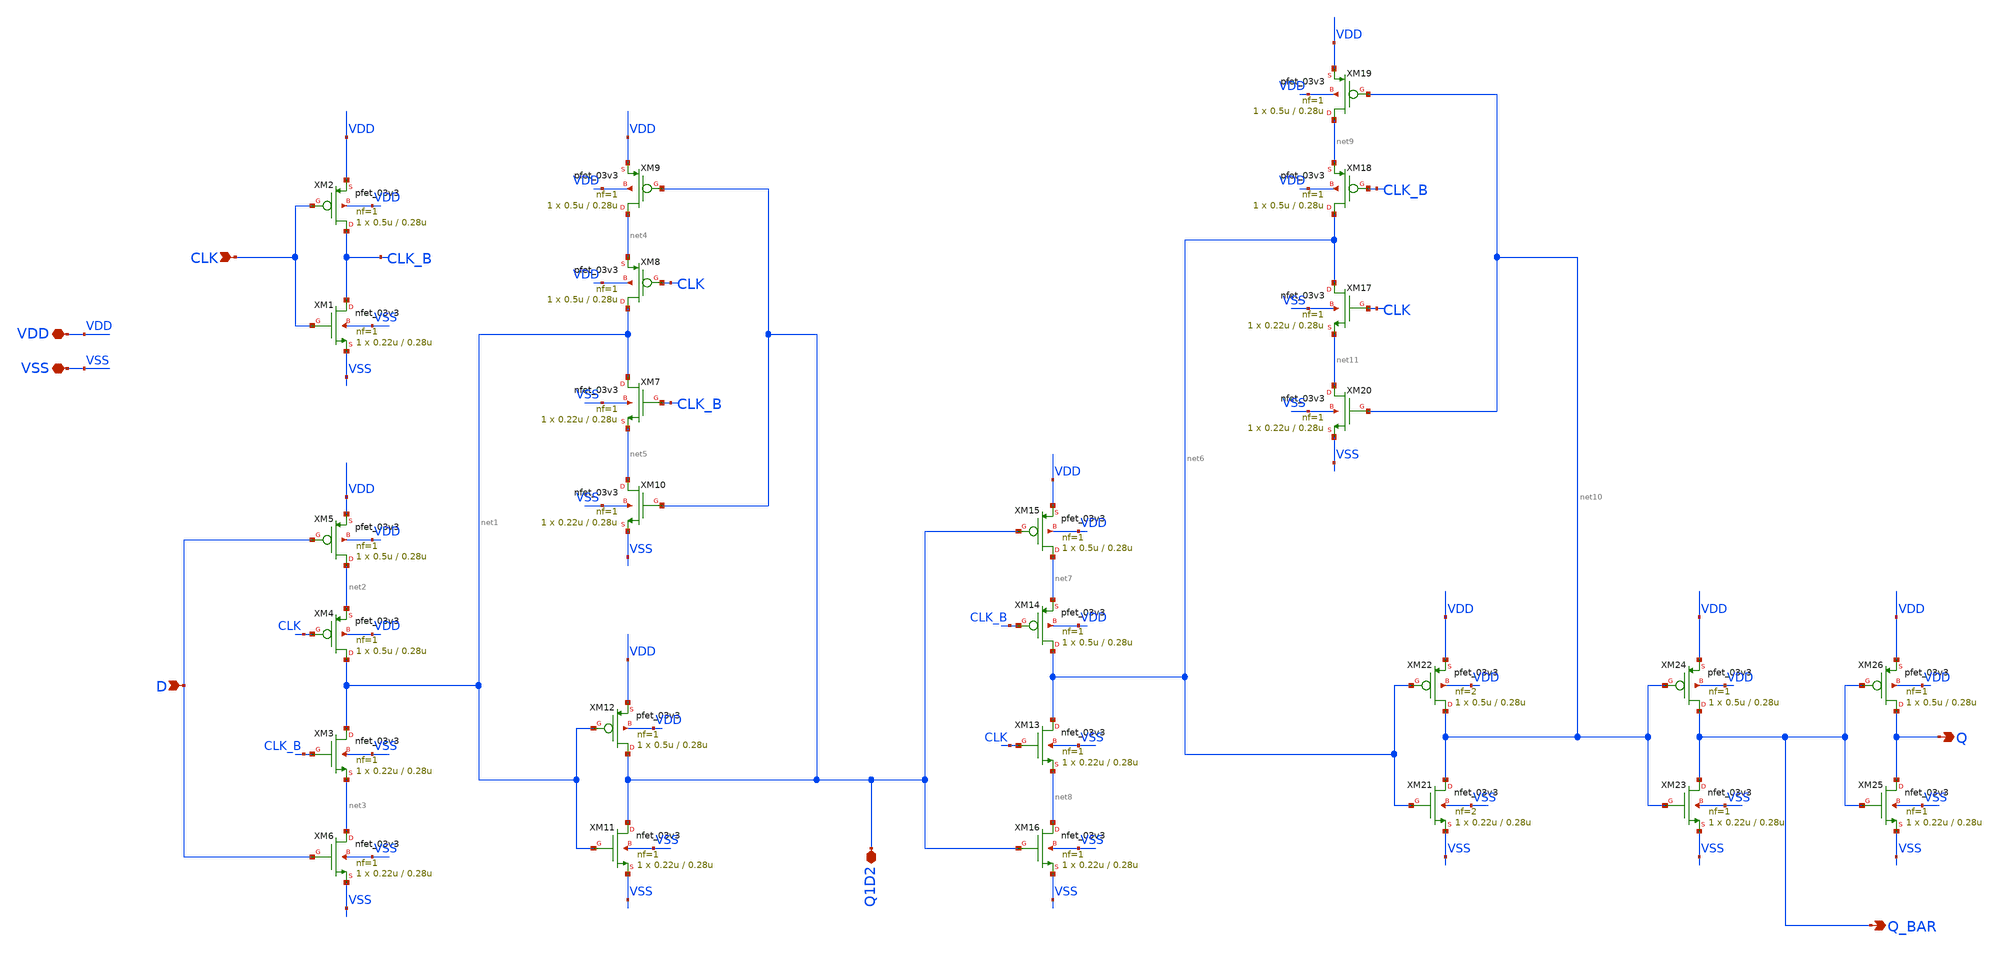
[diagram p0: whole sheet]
** sch_path: designs/libs/qw_core_analog/DFF_quizi.sch
**.subckt DFF_quizi CLK D Q_BAR VDD VSS Q Q1D2
*.ipin CLK
*.ipin D
*.opin Q_BAR
*.iopin VDD
*.iopin VSS
*.opin Q
*.iopin Q1D2
XM1 CLK_B CLK VSS VSS nfet_03v3 L=0.28u W=0.22u nf=1 ad='int((nf+1)/2) * W/nf * 0.18u' as='int((nf+2)/2) * W/nf * 0.18u'
+ pd='2*int((nf+1)/2) * (W/nf + 0.18u)' ps='2*int((nf+2)/2) * (W/nf + 0.18u)' nrd='0.18u / W' nrs='0.18u / W'
+ sa=0 sb=0 sd=0 m=1
XM2 CLK_B CLK VDD VDD pfet_03v3 L=0.28u W=0.5u nf=1 ad='int((nf+1)/2) * W/nf * 0.18u' as='int((nf+2)/2) * W/nf * 0.18u'
+ pd='2*int((nf+1)/2) * (W/nf + 0.18u)' ps='2*int((nf+2)/2) * (W/nf + 0.18u)' nrd='0.18u / W' nrs='0.18u / W'
+ sa=0 sb=0 sd=0 m=1
XM3 net1 CLK_B net3 VSS nfet_03v3 L=0.28u W=0.22u nf=1 ad='int((nf+1)/2) * W/nf * 0.18u' as='int((nf+2)/2) * W/nf * 0.18u'
+ pd='2*int((nf+1)/2) * (W/nf + 0.18u)' ps='2*int((nf+2)/2) * (W/nf + 0.18u)' nrd='0.18u / W' nrs='0.18u / W'
+ sa=0 sb=0 sd=0 m=1
XM4 net1 CLK net2 VDD pfet_03v3 L=0.28u W=0.5u nf=1 ad='int((nf+1)/2) * W/nf * 0.18u' as='int((nf+2)/2) * W/nf * 0.18u'
+ pd='2*int((nf+1)/2) * (W/nf + 0.18u)' ps='2*int((nf+2)/2) * (W/nf + 0.18u)' nrd='0.18u / W' nrs='0.18u / W'
+ sa=0 sb=0 sd=0 m=1
XM5 net2 D VDD VDD pfet_03v3 L=0.28u W=0.5u nf=1 ad='int((nf+1)/2) * W/nf * 0.18u' as='int((nf+2)/2) * W/nf * 0.18u'
+ pd='2*int((nf+1)/2) * (W/nf + 0.18u)' ps='2*int((nf+2)/2) * (W/nf + 0.18u)' nrd='0.18u / W' nrs='0.18u / W'
+ sa=0 sb=0 sd=0 m=1
XM6 net3 D VSS VSS nfet_03v3 L=0.28u W=0.22u nf=1 ad='int((nf+1)/2) * W/nf * 0.18u' as='int((nf+2)/2) * W/nf * 0.18u'
+ pd='2*int((nf+1)/2) * (W/nf + 0.18u)' ps='2*int((nf+2)/2) * (W/nf + 0.18u)' nrd='0.18u / W' nrs='0.18u / W'
+ sa=0 sb=0 sd=0 m=1
XM7 net1 CLK_B net5 VSS nfet_03v3 L=0.28u W=0.22u nf=1 ad='int((nf+1)/2) * W/nf * 0.18u' as='int((nf+2)/2) * W/nf * 0.18u'
+ pd='2*int((nf+1)/2) * (W/nf + 0.18u)' ps='2*int((nf+2)/2) * (W/nf + 0.18u)' nrd='0.18u / W' nrs='0.18u / W'
+ sa=0 sb=0 sd=0 m=1
XM8 net1 CLK net4 VDD pfet_03v3 L=0.28u W=0.5u nf=1 ad='int((nf+1)/2) * W/nf * 0.18u' as='int((nf+2)/2) * W/nf * 0.18u'
+ pd='2*int((nf+1)/2) * (W/nf + 0.18u)' ps='2*int((nf+2)/2) * (W/nf + 0.18u)' nrd='0.18u / W' nrs='0.18u / W'
+ sa=0 sb=0 sd=0 m=1
XM9 net4 Q1D2 VDD VDD pfet_03v3 L=0.28u W=0.5u nf=1 ad='int((nf+1)/2) * W/nf * 0.18u' as='int((nf+2)/2) * W/nf * 0.18u'
+ pd='2*int((nf+1)/2) * (W/nf + 0.18u)' ps='2*int((nf+2)/2) * (W/nf + 0.18u)' nrd='0.18u / W' nrs='0.18u / W'
+ sa=0 sb=0 sd=0 m=1
XM10 net5 Q1D2 VSS VSS nfet_03v3 L=0.28u W=0.22u nf=1 ad='int((nf+1)/2) * W/nf * 0.18u' as='int((nf+2)/2) * W/nf * 0.18u'
+ pd='2*int((nf+1)/2) * (W/nf + 0.18u)' ps='2*int((nf+2)/2) * (W/nf + 0.18u)' nrd='0.18u / W' nrs='0.18u / W'
+ sa=0 sb=0 sd=0 m=1
XM11 Q1D2 net1 VSS VSS nfet_03v3 L=0.28u W=0.22u nf=1 ad='int((nf+1)/2) * W/nf * 0.18u' as='int((nf+2)/2) * W/nf * 0.18u'
+ pd='2*int((nf+1)/2) * (W/nf + 0.18u)' ps='2*int((nf+2)/2) * (W/nf + 0.18u)' nrd='0.18u / W' nrs='0.18u / W'
+ sa=0 sb=0 sd=0 m=1
XM12 Q1D2 net1 VDD VDD pfet_03v3 L=0.28u W=0.5u nf=1 ad='int((nf+1)/2) * W/nf * 0.18u' as='int((nf+2)/2) * W/nf * 0.18u'
+ pd='2*int((nf+1)/2) * (W/nf + 0.18u)' ps='2*int((nf+2)/2) * (W/nf + 0.18u)' nrd='0.18u / W' nrs='0.18u / W'
+ sa=0 sb=0 sd=0 m=1
XM13 net6 CLK net8 VSS nfet_03v3 L=0.28u W=0.22u nf=1 ad='int((nf+1)/2) * W/nf * 0.18u' as='int((nf+2)/2) * W/nf * 0.18u'
+ pd='2*int((nf+1)/2) * (W/nf + 0.18u)' ps='2*int((nf+2)/2) * (W/nf + 0.18u)' nrd='0.18u / W' nrs='0.18u / W'
+ sa=0 sb=0 sd=0 m=1
XM14 net6 CLK_B net7 VDD pfet_03v3 L=0.28u W=0.5u nf=1 ad='int((nf+1)/2) * W/nf * 0.18u' as='int((nf+2)/2) * W/nf * 0.18u'
+ pd='2*int((nf+1)/2) * (W/nf + 0.18u)' ps='2*int((nf+2)/2) * (W/nf + 0.18u)' nrd='0.18u / W' nrs='0.18u / W'
+ sa=0 sb=0 sd=0 m=1
XM15 net7 Q1D2 VDD VDD pfet_03v3 L=0.28u W=0.5u nf=1 ad='int((nf+1)/2) * W/nf * 0.18u' as='int((nf+2)/2) * W/nf * 0.18u'
+ pd='2*int((nf+1)/2) * (W/nf + 0.18u)' ps='2*int((nf+2)/2) * (W/nf + 0.18u)' nrd='0.18u / W' nrs='0.18u / W'
+ sa=0 sb=0 sd=0 m=1
XM16 net8 Q1D2 VSS VSS nfet_03v3 L=0.28u W=0.22u nf=1 ad='int((nf+1)/2) * W/nf * 0.18u' as='int((nf+2)/2) * W/nf * 0.18u'
+ pd='2*int((nf+1)/2) * (W/nf + 0.18u)' ps='2*int((nf+2)/2) * (W/nf + 0.18u)' nrd='0.18u / W' nrs='0.18u / W'
+ sa=0 sb=0 sd=0 m=1
XM17 net6 CLK net11 VSS nfet_03v3 L=0.28u W=0.22u nf=1 ad='int((nf+1)/2) * W/nf * 0.18u' as='int((nf+2)/2) * W/nf * 0.18u'
+ pd='2*int((nf+1)/2) * (W/nf + 0.18u)' ps='2*int((nf+2)/2) * (W/nf + 0.18u)' nrd='0.18u / W' nrs='0.18u / W'
+ sa=0 sb=0 sd=0 m=1
XM18 net6 CLK_B net9 VDD pfet_03v3 L=0.28u W=0.5u nf=1 ad='int((nf+1)/2) * W/nf * 0.18u' as='int((nf+2)/2) * W/nf * 0.18u'
+ pd='2*int((nf+1)/2) * (W/nf + 0.18u)' ps='2*int((nf+2)/2) * (W/nf + 0.18u)' nrd='0.18u / W' nrs='0.18u / W'
+ sa=0 sb=0 sd=0 m=1
XM19 net9 net10 VDD VDD pfet_03v3 L=0.28u W=0.5u nf=1 ad='int((nf+1)/2) * W/nf * 0.18u' as='int((nf+2)/2) * W/nf * 0.18u'
+ pd='2*int((nf+1)/2) * (W/nf + 0.18u)' ps='2*int((nf+2)/2) * (W/nf + 0.18u)' nrd='0.18u / W' nrs='0.18u / W'
+ sa=0 sb=0 sd=0 m=1
XM20 net11 net10 VSS VSS nfet_03v3 L=0.28u W=0.22u nf=1 ad='int((nf+1)/2) * W/nf * 0.18u' as='int((nf+2)/2) * W/nf * 0.18u'
+ pd='2*int((nf+1)/2) * (W/nf + 0.18u)' ps='2*int((nf+2)/2) * (W/nf + 0.18u)' nrd='0.18u / W' nrs='0.18u / W'
+ sa=0 sb=0 sd=0 m=1
XM21 net10 net6 VSS VSS nfet_03v3 L=0.28u W=0.22u nf=2 ad='int((nf+1)/2) * W/nf * 0.18u' as='int((nf+2)/2) * W/nf * 0.18u'
+ pd='2*int((nf+1)/2) * (W/nf + 0.18u)' ps='2*int((nf+2)/2) * (W/nf + 0.18u)' nrd='0.18u / W' nrs='0.18u / W'
+ sa=0 sb=0 sd=0 m=1
XM22 net10 net6 VDD VDD pfet_03v3 L=0.28u W=0.5u nf=2 ad='int((nf+1)/2) * W/nf * 0.18u' as='int((nf+2)/2) * W/nf * 0.18u'
+ pd='2*int((nf+1)/2) * (W/nf + 0.18u)' ps='2*int((nf+2)/2) * (W/nf + 0.18u)' nrd='0.18u / W' nrs='0.18u / W'
+ sa=0 sb=0 sd=0 m=1
XM23 Q_BAR net10 VSS VSS nfet_03v3 L=0.28u W=0.22u nf=1 ad='int((nf+1)/2) * W/nf * 0.18u' as='int((nf+2)/2) * W/nf * 0.18u'
+ pd='2*int((nf+1)/2) * (W/nf + 0.18u)' ps='2*int((nf+2)/2) * (W/nf + 0.18u)' nrd='0.18u / W' nrs='0.18u / W'
+ sa=0 sb=0 sd=0 m=1
XM24 Q_BAR net10 VDD VDD pfet_03v3 L=0.28u W=0.5u nf=1 ad='int((nf+1)/2) * W/nf * 0.18u' as='int((nf+2)/2) * W/nf * 0.18u'
+ pd='2*int((nf+1)/2) * (W/nf + 0.18u)' ps='2*int((nf+2)/2) * (W/nf + 0.18u)' nrd='0.18u / W' nrs='0.18u / W'
+ sa=0 sb=0 sd=0 m=1
XM25 Q Q_BAR VSS VSS nfet_03v3 L=0.28u W=0.22u nf=1 ad='int((nf+1)/2) * W/nf * 0.18u' as='int((nf+2)/2) * W/nf * 0.18u'
+ pd='2*int((nf+1)/2) * (W/nf + 0.18u)' ps='2*int((nf+2)/2) * (W/nf + 0.18u)' nrd='0.18u / W' nrs='0.18u / W'
+ sa=0 sb=0 sd=0 m=1
XM26 Q Q_BAR VDD VDD pfet_03v3 L=0.28u W=0.5u nf=1 ad='int((nf+1)/2) * W/nf * 0.18u' as='int((nf+2)/2) * W/nf * 0.18u'
+ pd='2*int((nf+1)/2) * (W/nf + 0.18u)' ps='2*int((nf+2)/2) * (W/nf + 0.18u)' nrd='0.18u / W' nrs='0.18u / W'
+ sa=0 sb=0 sd=0 m=1
**.ends
.end
